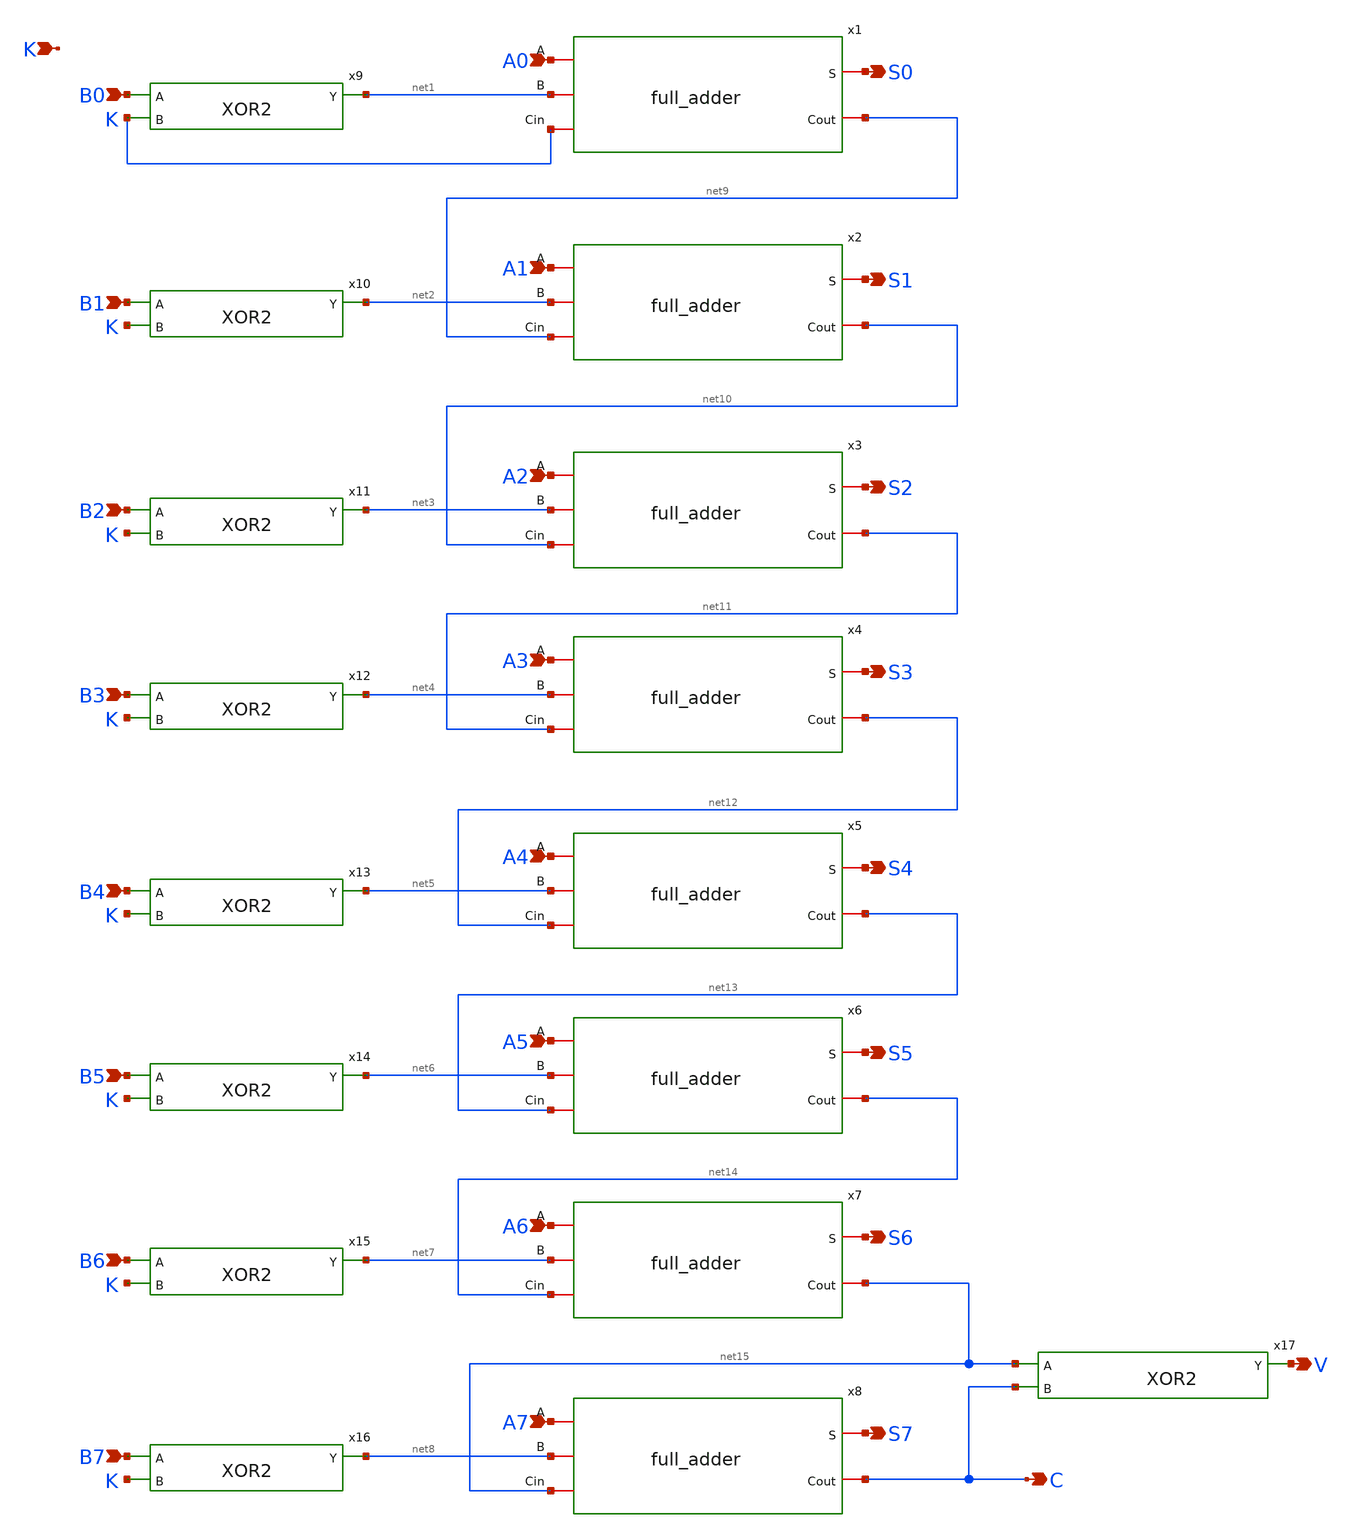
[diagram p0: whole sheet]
** sch_path: design/xschem/SUBTRACTOR/8-bit_adder_subtractor.sch
**.subckt 8-bit_adder_subtractor A0 B0 S0 K A1 B1 S1 A2 B2 S2 A3 B3 S3 A4 B4 S4 A5 B5 S5 A6 B6 S6 A7
*+ B7 S7 C V
*.ipin A0
*.ipin B0
*.opin S0
*.ipin K
*.ipin A1
*.ipin B1
*.opin S1
*.ipin A2
*.ipin B2
*.opin S2
*.ipin A3
*.ipin B3
*.opin S3
*.ipin A4
*.ipin B4
*.opin S4
*.ipin A5
*.ipin B5
*.opin S5
*.ipin A6
*.ipin B6
*.opin S6
*.ipin A7
*.ipin B7
*.opin S7
*.opin C
*.opin V
x2 A1 S1 net2 net9 net10 full_adder
x3 A2 S2 net3 net10 net11 full_adder
x4 A3 S3 net4 net11 net12 full_adder
x5 A4 S4 net5 net12 net13 full_adder
x6 A5 S5 net6 net13 net14 full_adder
x7 A6 S6 net7 net14 net15 full_adder
x8 A7 S7 net8 net15 C full_adder
x9 B0 K net1 VSS VDD XOR2
x10 B1 K net2 VSS VDD XOR2
x11 B2 K net3 VSS VDD XOR2
x12 B3 K net4 VSS VDD XOR2
x13 B4 K net5 VSS VDD XOR2
x14 B5 K net6 VSS VDD XOR2
x15 B6 K net7 VSS VDD XOR2
x16 B7 K net8 VSS VDD XOR2
x1 A0 S0 net1 K net9 full_adder
x17 net15 C V VSS VDD XOR2
**.ends
.end
